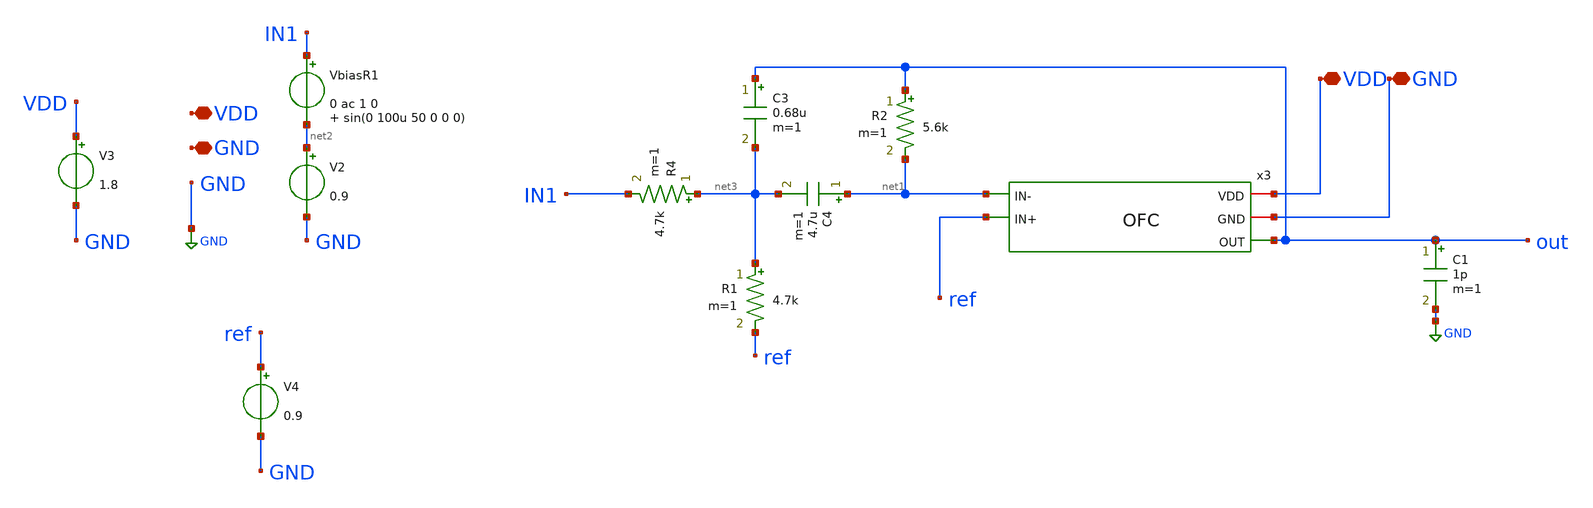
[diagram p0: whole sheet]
** sch_path: xschem/untitled-2.sch
**.subckt untitled-2 VDD GND VDD GND
*.iopin VDD
*.iopin GND
*.iopin VDD
*.iopin GND
x3 VDD GND out net1 ref OFC
V3 VDD GND 1.8
VbiasR1 IN1 net2 0 ac 1 0 sin(0 100u 50 0 0 0)
V2 net2 GND 0.9
C1 out GND 1p m=1
V4 ref GND 0.9
C3 out net3 0.68u m=1
C4 net1 net3 4.7u m=1
R4 net3 IN1 4.7k m=1
R1 net3 ref 4.7k m=1
R2 out net1 5.6k m=1
**** begin user architecture code



.option reltol=1e-5   abstol=1e-14 savecurrents
.control
  save all
  op
  remzerovec
  write InstrumentationalAmplifier.raw

  set appendwrite
  ac dec 10 1 1e9
  remzerovec
  write InstrumentationalAmplifier.raw

  tran 100u 100m
  write InstrumentationalAmplifier.raw

  set appendwrite
  noise v(out1) VbiasR1 dec 10 0.05 1e3
  remzerovec
  write InstrumentationalAmplifier.raw
  setplot noise1
  plot inoise_spectrum

.endc



.lib $::SKYWATER_MODELS/sky130.lib.spice tt
**** end user architecture code
**.ends

* expanding   symbol:  OFC.sym # of pins=5
** sym_path: OFC.sym
** sch_path: OFC.sch
.subckt OFC VDD GND OUT IN- IN+
*.iopin VDD
*.iopin GND
*.ipin IN+
*.ipin IN-
*.opin OUT
XM11 S Vb VDD VDD sky130_fd_pr__pfet_01v8_lvt L=1 W=60 nf=2 ad='int((nf+1)/2) * W/nf * 0.29' as='int((nf+2)/2) * W/nf * 0.29'
+ pd='2*int((nf+1)/2) * (W/nf + 0.29)' ps='2*int((nf+2)/2) * (W/nf + 0.29)' nrd='0.29 / W' nrs='0.29 / W'
+ sa=0 sb=0 sd=0 mult=2 m=2
XM1 D1 IN+ S S sky130_fd_pr__pfet_01v8_lvt L=10 W=25 nf=2 ad='int((nf+1)/2) * W/nf * 0.29' as='int((nf+2)/2) * W/nf * 0.29'
+ pd='2*int((nf+1)/2) * (W/nf + 0.29)' ps='2*int((nf+2)/2) * (W/nf + 0.29)' nrd='0.29 / W' nrs='0.29 / W'
+ sa=0 sb=0 sd=0 mult=2 m=2
XM2 D2 IN- S S sky130_fd_pr__pfet_01v8_lvt L=10 W=25 nf=2 ad='int((nf+1)/2) * W/nf * 0.29' as='int((nf+2)/2) * W/nf * 0.29'
+ pd='2*int((nf+1)/2) * (W/nf + 0.29)' ps='2*int((nf+2)/2) * (W/nf + 0.29)' nrd='0.29 / W' nrs='0.29 / W'
+ sa=0 sb=0 sd=0 mult=2 m=2
XM3 OUT Vc1 D2 GND sky130_fd_pr__nfet_01v8_lvt L=1 W=4 nf=1 ad='int((nf+1)/2) * W/nf * 0.29' as='int((nf+2)/2) * W/nf * 0.29'
+ pd='2*int((nf+1)/2) * (W/nf + 0.29)' ps='2*int((nf+2)/2) * (W/nf + 0.29)' nrd='0.29 / W' nrs='0.29 / W'
+ sa=0 sb=0 sd=0 mult=1 m=1
XM4 D2 Vc GND GND sky130_fd_pr__nfet_01v8_lvt L=1 W=2.8 nf=1 ad='int((nf+1)/2) * W/nf * 0.29' as='int((nf+2)/2) * W/nf * 0.29'
+ pd='2*int((nf+1)/2) * (W/nf + 0.29)' ps='2*int((nf+2)/2) * (W/nf + 0.29)' nrd='0.29 / W' nrs='0.29 / W'
+ sa=0 sb=0 sd=0 mult=1 m=1
XM5 D1 Vc GND GND sky130_fd_pr__nfet_01v8_lvt L=1 W=2.8 nf=1 ad='int((nf+1)/2) * W/nf * 0.29' as='int((nf+2)/2) * W/nf * 0.29'
+ pd='2*int((nf+1)/2) * (W/nf + 0.29)' ps='2*int((nf+2)/2) * (W/nf + 0.29)' nrd='0.29 / W' nrs='0.29 / W'
+ sa=0 sb=0 sd=0 mult=1 m=1
XM6 G Vc1 D1 GND sky130_fd_pr__nfet_01v8_lvt L=1 W=4 nf=1 ad='int((nf+1)/2) * W/nf * 0.29' as='int((nf+2)/2) * W/nf * 0.29'
+ pd='2*int((nf+1)/2) * (W/nf + 0.29)' ps='2*int((nf+2)/2) * (W/nf + 0.29)' nrd='0.29 / W' nrs='0.29 / W'
+ sa=0 sb=0 sd=0 mult=1 m=1
XM7 G Vc2 D9 D9 sky130_fd_pr__pfet_01v8_lvt L=2.23 W=3 nf=1 ad='int((nf+1)/2) * W/nf * 0.29' as='int((nf+2)/2) * W/nf * 0.29'
+ pd='2*int((nf+1)/2) * (W/nf + 0.29)' ps='2*int((nf+2)/2) * (W/nf + 0.29)' nrd='0.29 / W' nrs='0.29 / W'
+ sa=0 sb=0 sd=0 mult=1 m=1
XM9 D9 G VDD VDD sky130_fd_pr__pfet_01v8_lvt L=2.23 W=4 nf=1 ad='int((nf+1)/2) * W/nf * 0.29' as='int((nf+2)/2) * W/nf * 0.29'
+ pd='2*int((nf+1)/2) * (W/nf + 0.29)' ps='2*int((nf+2)/2) * (W/nf + 0.29)' nrd='0.29 / W' nrs='0.29 / W'
+ sa=0 sb=0 sd=0 mult=1 m=1
XM8 D10 G VDD VDD sky130_fd_pr__pfet_01v8_lvt L=2.23 W=4 nf=1 ad='int((nf+1)/2) * W/nf * 0.29' as='int((nf+2)/2) * W/nf * 0.29'
+ pd='2*int((nf+1)/2) * (W/nf + 0.29)' ps='2*int((nf+2)/2) * (W/nf + 0.29)' nrd='0.29 / W' nrs='0.29 / W'
+ sa=0 sb=0 sd=0 mult=1 m=1
XM10 OUT Vc2 D10 D10 sky130_fd_pr__pfet_01v8_lvt L=2.23 W=3 nf=1 ad='int((nf+1)/2) * W/nf * 0.29' as='int((nf+2)/2) * W/nf * 0.29'
+ pd='2*int((nf+1)/2) * (W/nf + 0.29)' ps='2*int((nf+2)/2) * (W/nf + 0.29)' nrd='0.29 / W' nrs='0.29 / W'
+ sa=0 sb=0 sd=0 mult=1 m=1
XR2 Vb VDD GND sky130_fd_pr__res_xhigh_po_0p35 L=5 mult=1 m=1
XR3 GND Vb GND sky130_fd_pr__res_xhigh_po_0p35 L=13.2 mult=1 m=1
XR1 Vc VDD GND sky130_fd_pr__res_xhigh_po_0p35 L=5 mult=1 m=1
XR4 GND Vc GND sky130_fd_pr__res_xhigh_po_0p35 L=3.07 mult=1 m=1
XR5 Vc1 VDD GND sky130_fd_pr__res_xhigh_po_0p35 L=5 mult=1 m=1
XR6 GND Vc1 GND sky130_fd_pr__res_xhigh_po_0p35 L=13.2 mult=1 m=1
XR7 Vc2 VDD GND sky130_fd_pr__res_xhigh_po_0p35 L=5 mult=1 m=1
XR8 GND Vc2 GND sky130_fd_pr__res_xhigh_po_0p35 L=1.6 mult=1 m=1
.ends

.GLOBAL GND
.end
